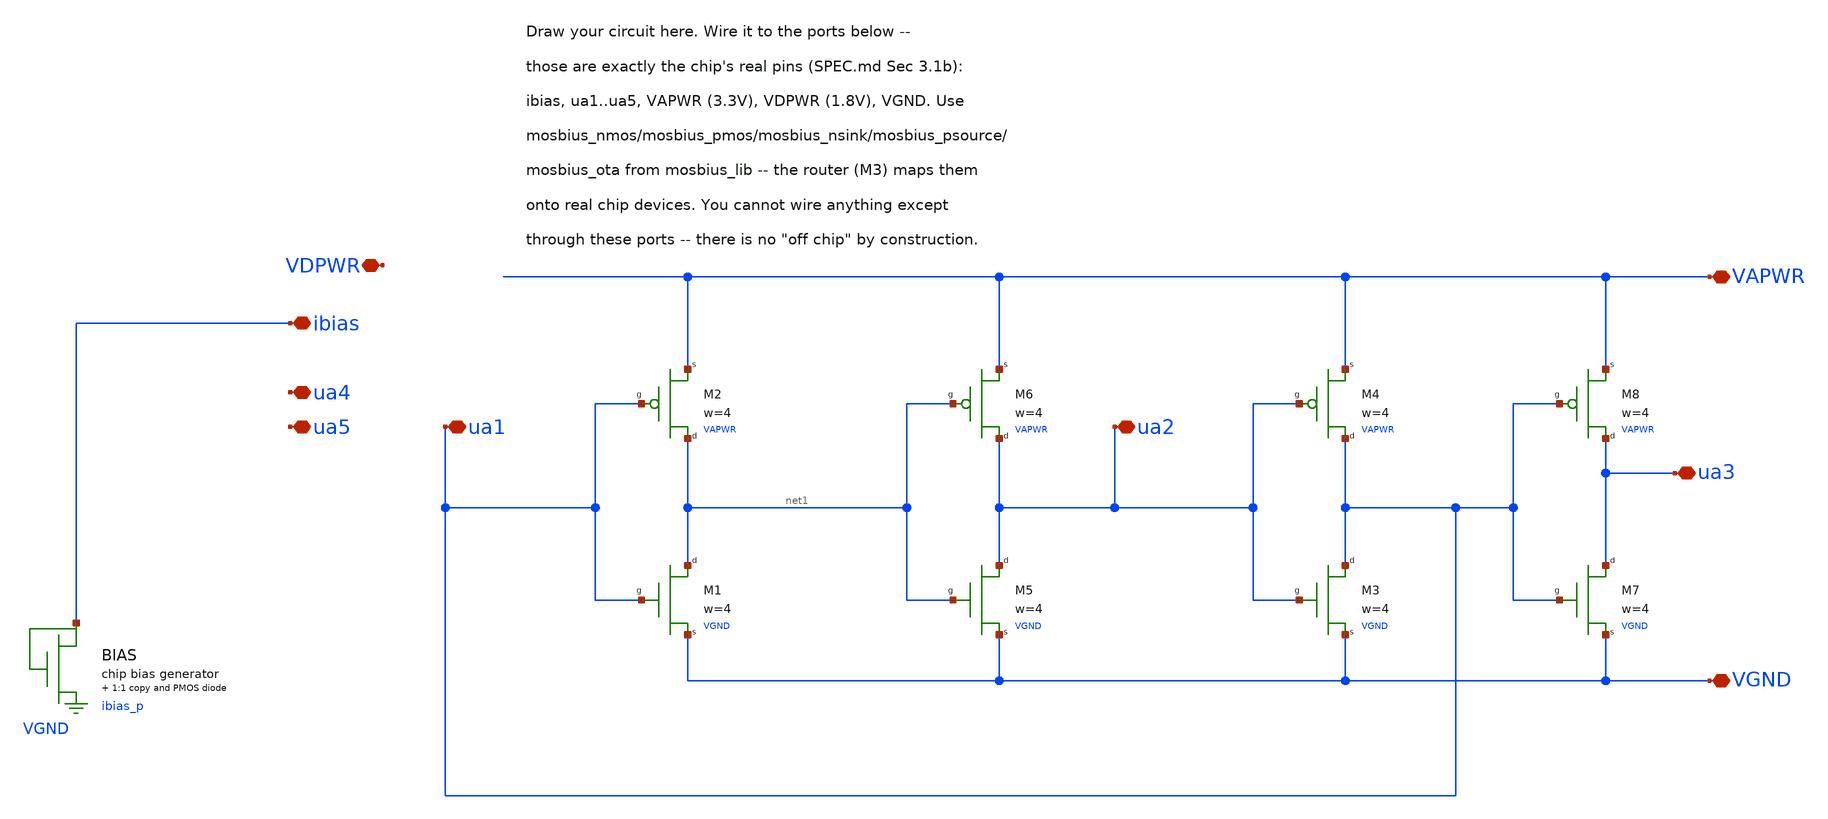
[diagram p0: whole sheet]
** sch_path: examples/ringosc/ring.sch
**.subckt ring ibias ua1 ua2 ua3 ua5 VAPWR VDPWR VGND ua4
*.iopin ibias
*.iopin ua1
*.iopin ua2
*.iopin ua3
*.iopin ua5
*.iopin VAPWR
*.iopin VDPWR
*.iopin VGND
*.iopin ua4
XM1 ua1 net1 VGND VGND mosbius_nmos w=4
M2 ua1 net1 VAPWR VAPWR mosbius_pmos w=4
XM3 ua2 ua1 VGND VGND mosbius_nmos w=4
M4 ua2 ua1 VAPWR VAPWR mosbius_pmos w=4
XM5 net1 ua2 VGND VGND mosbius_nmos w=4
M6 net1 ua2 VAPWR VAPWR mosbius_pmos w=4
XM7 ua1 ua3 VGND VGND mosbius_nmos w=4
M8 ua1 ua3 VAPWR VAPWR mosbius_pmos w=4
XBIAS ibias ibias_p VGND VAPWR mosbius_bias
**.ends

* expanding   symbol:  mosbius_nmos.sym # of pins=3
** sym_path: xschem/mosbius_lib/mosbius_nmos.sym
** sch_path: xschem/mosbius_lib/mosbius_nmos.sch
.subckt mosbius_nmos g d s b  w=1
*.iopin s
*.ipin g
*.iopin d
XM1 d g s well sky130_fd_pr__nfet_g5v0d10v5 L=0.5 W=wdev nf=nfdev ad='int((nf+1)/2) * W/nf * 0.29' as='int((nf+2)/2) * W/nf * 0.29'
+ pd='2*int((nf+1)/2) * (W/nf + 0.29)' ps='2*int((nf+2)/2) * (W/nf + 0.29)' nrd='0.29 / W' nrs='0.29 / W'
+ sa=0 sb=0 sd=0 mult=1 m=1
**** begin user architecture code

.param wdev='10*w' nfdev='2*w'

**** end user architecture code
Rwell_source well s 'rwell_source' m=1
Rwell_rail well b 'rwell_rail' m=1
* implicit port xxx
.ends


* expanding   symbol:  mosbius_pmos.sym # of pins=3
** sym_path: xschem/mosbius_lib/mosbius_pmos.sym
** sch_path: xschem/mosbius_lib/mosbius_pmos.sch
.subckt mosbius_pmos g d s b  w=1
*.iopin s
*.ipin g
*.iopin d
XM1 d g s well sky130_fd_pr__pfet_g5v0d10v5 L=0.5 W=wdev nf=nfdev ad='int((nf+1)/2) * W/nf * 0.29' as='int((nf+2)/2) * W/nf * 0.29'
+ pd='2*int((nf+1)/2) * (W/nf + 0.29)' ps='2*int((nf+2)/2) * (W/nf + 0.29)' nrd='0.29 / W' nrs='0.29 / W'
+ sa=0 sb=0 sd=0 mult=1 m=1
**** begin user architecture code

.param wdev='30*w' nfdev='wdev/pmos_width_per_finger'

**** end user architecture code
Rwell_source well s 'rwell_source' m=1
Rwell_rail well b 'rwell_rail' m=1
* implicit port xxx
.ends


* expanding   symbol:  mosbius_bias.sym # of pins=1
** sym_path: xschem/mosbius_lib/mosbius_bias.sym
** sch_path: xschem/mosbius_lib/mosbius_bias.sch
.subckt mosbius_bias ibias ibias_p bn bp
*.iopin ibias
XMbias_ref ibias ibias bn bn sky130_fd_pr__nfet_g5v0d10v5 L=1 W=10 nf=2 ad='int((nf+1)/2) * W/nf * 0.29'
+ as='int((nf+2)/2) * W/nf * 0.29' pd='2*int((nf+1)/2) * (W/nf + 0.29)' ps='2*int((nf+2)/2) * (W/nf + 0.29)'
+ nrd='0.29 / W' nrs='0.29 / W' sa=0 sb=0 sd=0 mult=1 m=1
XMbias_copy ibias_p ibias bn bn sky130_fd_pr__nfet_g5v0d10v5 L=1 W=10 nf=2 ad='int((nf+1)/2) * W/nf * 0.29'
+ as='int((nf+2)/2) * W/nf * 0.29' pd='2*int((nf+1)/2) * (W/nf + 0.29)' ps='2*int((nf+2)/2) * (W/nf + 0.29)'
+ nrd='0.29 / W' nrs='0.29 / W' sa=0 sb=0 sd=0 mult=1 m=1
XMbias_p ibias_p ibias_p bp bp sky130_fd_pr__pfet_g5v0d10v5 L=1 W=30 nf=30/pmos_width_per_finger ad='int((nf+1)/2) * W/nf * 0.29'
+ as='int((nf+2)/2) * W/nf * 0.29' pd='2*int((nf+1)/2) * (W/nf + 0.29)' ps='2*int((nf+2)/2) * (W/nf + 0.29)'
+ nrd='0.29 / W' nrs='0.29 / W' sa=0 sb=0 sd=0 mult=1 m=1
* implicit port xxx
.ends

.end
